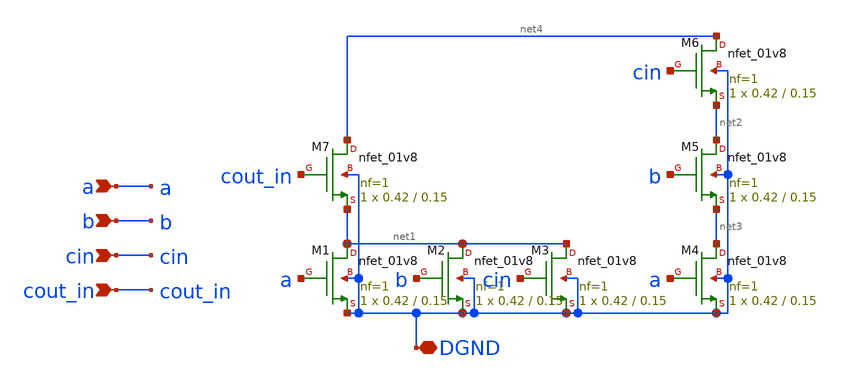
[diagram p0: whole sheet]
** sch_path: tut6/incr/step2/fa.sch
**.subckt fa a b cin DGND cout_in
*.ipin a
*.ipin b
*.ipin cin
*.iopin DGND
*.ipin cout_in
XM1 net1 a DGND DGND sky130_fd_pr__nfet_01v8 L=0.15 W=0.42 nf=1 ad='int((nf+1)/2) * W/nf * 0.29' as='int((nf+2)/2) * W/nf * 0.29'
+ pd='2*int((nf+1)/2) * (W/nf + 0.29)' ps='2*int((nf+2)/2) * (W/nf + 0.29)' nrd='0.29 / W' nrs='0.29 / W'
+ sa=0 sb=0 sd=0 mult=1 m=1
XM2 net1 b DGND DGND sky130_fd_pr__nfet_01v8 L=0.15 W=0.42 nf=1 ad='int((nf+1)/2) * W/nf * 0.29' as='int((nf+2)/2) * W/nf * 0.29'
+ pd='2*int((nf+1)/2) * (W/nf + 0.29)' ps='2*int((nf+2)/2) * (W/nf + 0.29)' nrd='0.29 / W' nrs='0.29 / W'
+ sa=0 sb=0 sd=0 mult=1 m=1
XM3 net1 cin DGND DGND sky130_fd_pr__nfet_01v8 L=0.15 W=0.42 nf=1 ad='int((nf+1)/2) * W/nf * 0.29' as='int((nf+2)/2) * W/nf * 0.29'
+ pd='2*int((nf+1)/2) * (W/nf + 0.29)' ps='2*int((nf+2)/2) * (W/nf + 0.29)' nrd='0.29 / W' nrs='0.29 / W'
+ sa=0 sb=0 sd=0 mult=1 m=1
XM4 net3 a DGND DGND sky130_fd_pr__nfet_01v8 L=0.15 W=0.42 nf=1 ad='int((nf+1)/2) * W/nf * 0.29' as='int((nf+2)/2) * W/nf * 0.29'
+ pd='2*int((nf+1)/2) * (W/nf + 0.29)' ps='2*int((nf+2)/2) * (W/nf + 0.29)' nrd='0.29 / W' nrs='0.29 / W'
+ sa=0 sb=0 sd=0 mult=1 m=1
XM5 net2 b net3 DGND sky130_fd_pr__nfet_01v8 L=0.15 W=0.42 nf=1 ad='int((nf+1)/2) * W/nf * 0.29' as='int((nf+2)/2) * W/nf * 0.29'
+ pd='2*int((nf+1)/2) * (W/nf + 0.29)' ps='2*int((nf+2)/2) * (W/nf + 0.29)' nrd='0.29 / W' nrs='0.29 / W'
+ sa=0 sb=0 sd=0 mult=1 m=1
XM6 net4 cin net2 DGND sky130_fd_pr__nfet_01v8 L=0.15 W=0.42 nf=1 ad='int((nf+1)/2) * W/nf * 0.29' as='int((nf+2)/2) * W/nf * 0.29'
+ pd='2*int((nf+1)/2) * (W/nf + 0.29)' ps='2*int((nf+2)/2) * (W/nf + 0.29)' nrd='0.29 / W' nrs='0.29 / W'
+ sa=0 sb=0 sd=0 mult=1 m=1
XM7 net4 cout_in net1 DGND sky130_fd_pr__nfet_01v8 L=0.15 W=0.42 nf=1 ad='int((nf+1)/2) * W/nf * 0.29'
+ as='int((nf+2)/2) * W/nf * 0.29' pd='2*int((nf+1)/2) * (W/nf + 0.29)' ps='2*int((nf+2)/2) * (W/nf + 0.29)'
+ nrd='0.29 / W' nrs='0.29 / W' sa=0 sb=0 sd=0 mult=1 m=1
**.ends
.end
